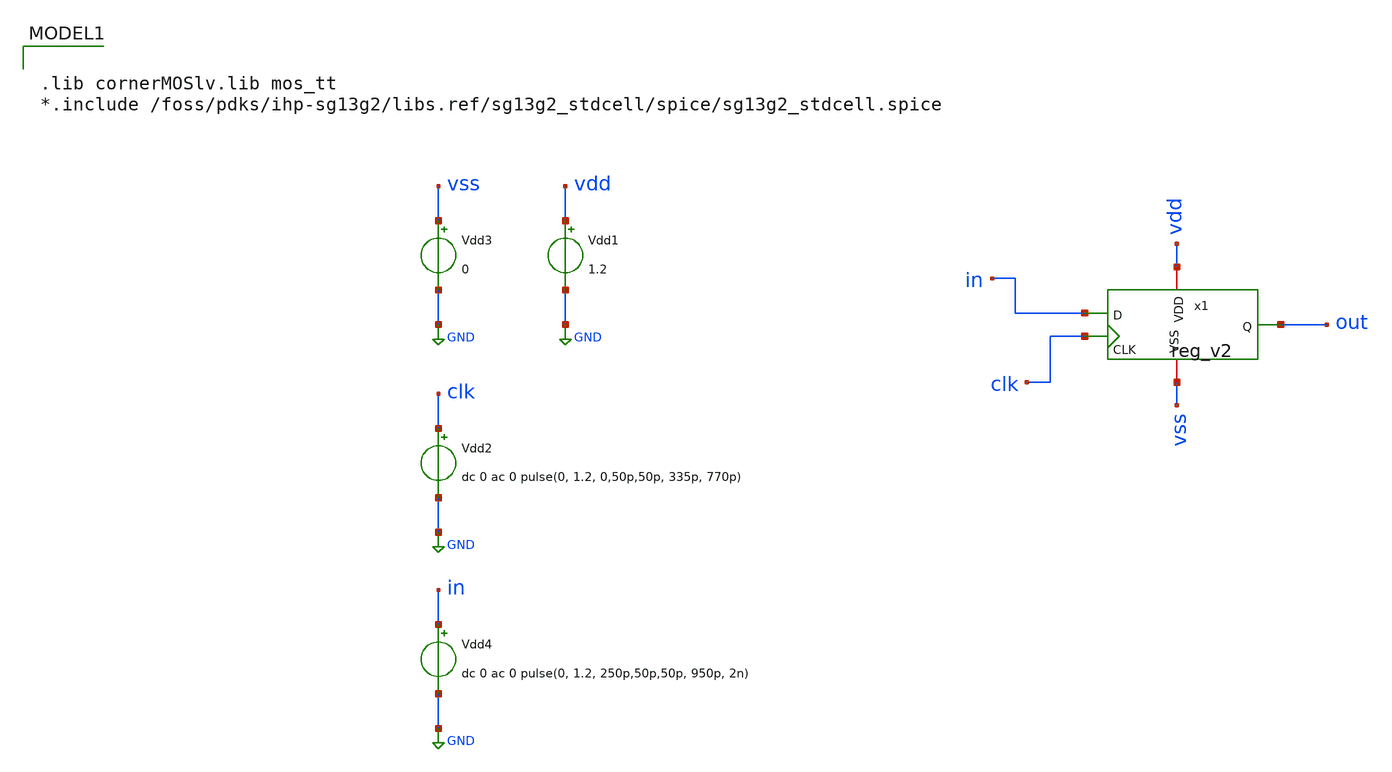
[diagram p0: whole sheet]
** sch_path: verification/testbenches/tb_reg.sch
**.subckt tb_reg
Vdd1 vdd GND 1.2
Vdd3 vss GND 0
Vdd2 clk GND dc 0 ac 0 pulse(0, 1.2, 0,50p,50p, 335p, 770p)
Vdd4 in GND dc 0 ac 0 pulse(0, 1.2, 250p,50p,50p, 950p, 2n)
x1 vdd clk vss out in reg_v2
**** begin user architecture code

.lib cornerMOSlv.lib mos_tt
*.include /foss/pdks/ihp-sg13g2/libs.ref/sg13g2_stdcell/spice/sg13g2_stdcell.spice




.save v(clk) v(in) v(out)


.tran 5p 6n

.control
run
set color0=white
write tran_logic.raw

.endc


**** end user architecture code
**.ends
.GLOBAL GND
.end
